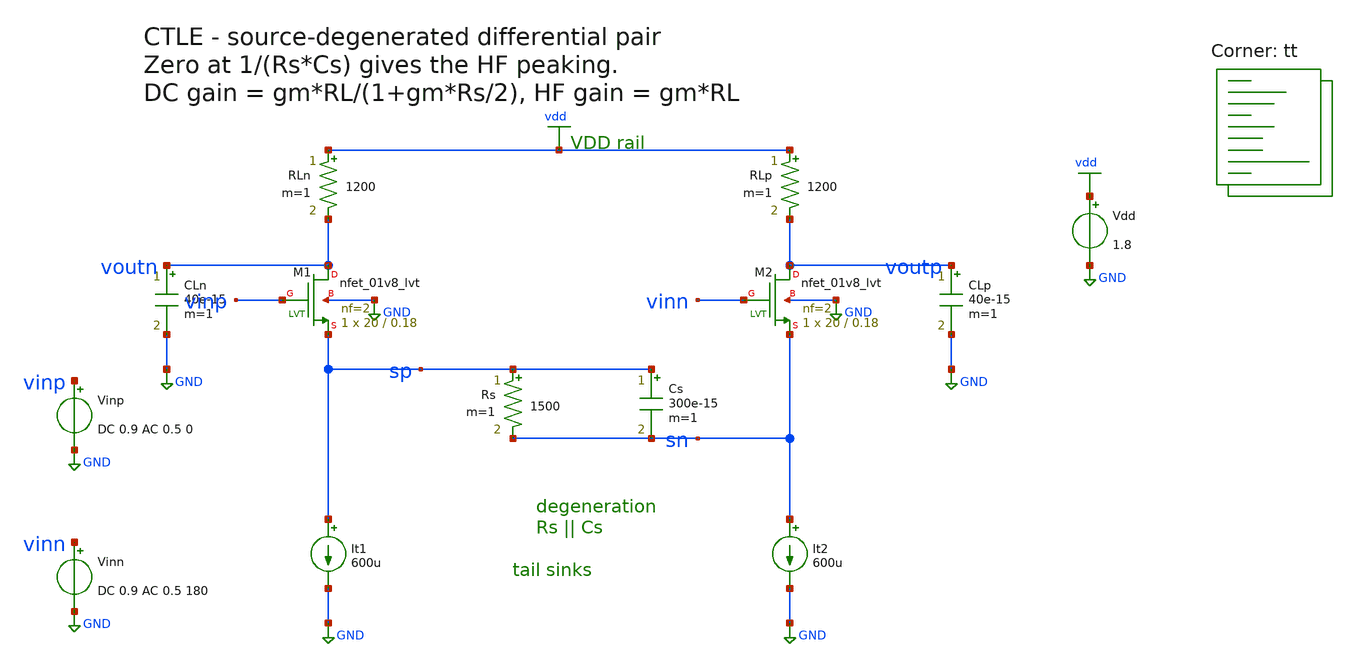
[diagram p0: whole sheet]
** sch_path: netlists/ctle_tb.sch
**.subckt ctle_tb
XM1 voutn vinp sp GND sky130_fd_pr__nfet_01v8_lvt L=0.18 W=20 nf=2 ad=0 as=0 pd=0 ps=0 nrd=0 nrs=0
+ sa=0 sb=0 sd=0 mult=1 m=1
XM2 voutp vinn sn GND sky130_fd_pr__nfet_01v8_lvt L=0.18 W=20 nf=2 ad=0 as=0 pd=0 ps=0 nrd=0 nrs=0
+ sa=0 sb=0 sd=0 mult=1 m=1
RLn vdd voutn 1200 m=1
RLp vdd voutp 1200 m=1
Rs sp sn 1500 m=1
Cs sp sn 300e-15 m=1
CLn voutn GND 40e-15 m=1
CLp voutp GND 40e-15 m=1
It1 sp GND 600u
It2 sn GND 600u
Vdd vdd GND 1.8
Vinp vinp GND DC 0.9 AC 0.5 0
Vinn vinn GND DC 0.9 AC 0.5 180
**** begin user architecture code
.lib $::SKYWATER_MODELS/sky130.lib.spice tt
**** end user architecture code
**.ends
.GLOBAL vdd
.GLOBAL GND
**** begin user architecture code

.control
save all
op
echo ---------- BIAS (want vds > vdsat) ----------
print @m.xm1.msky130_fd_pr__nfet_01v8_lvt[id]
print @m.xm1.msky130_fd_pr__nfet_01v8_lvt[gm]
print @m.xm1.msky130_fd_pr__nfet_01v8_lvt[vds]
print @m.xm1.msky130_fd_pr__nfet_01v8_lvt[vdsat]
ac dec 40 1e6 20e9
let g = vdb(voutp,voutn)
echo ---------- AC (expect peaking ~10.1 dB) ----------
print g[0]
print maximum(g)
plot g
.endc


**** end user architecture code
.end
